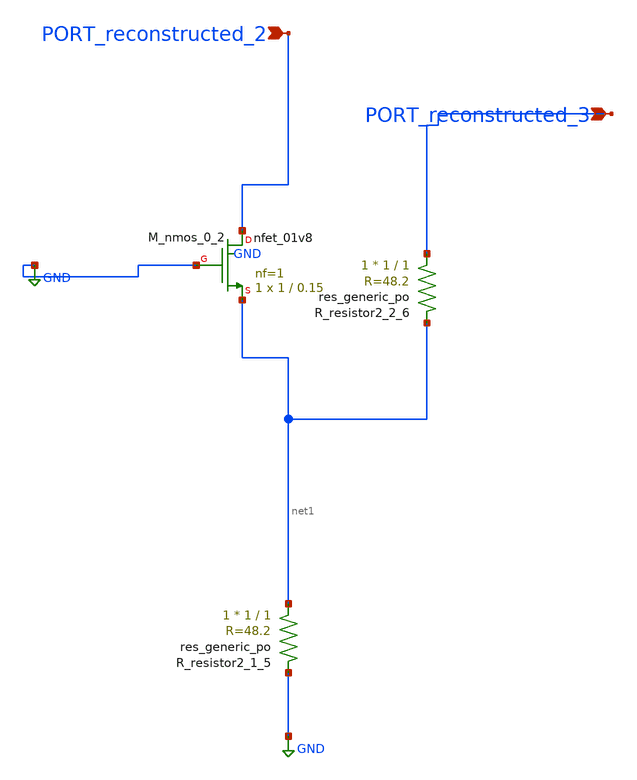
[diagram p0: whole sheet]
** sch_path: schematics/AMSNet/93.sch
**.subckt 93 PORT_reconstructed_2 PORT_reconstructed_3
*.ipin PORT_reconstructed_2
*.ipin PORT_reconstructed_3
XM_nmos_0_2 PORT_reconstructed_2 GND net1 GND sky130_fd_pr__nfet_01v8 L=0.15 W=1 nf=1 ad='int((1 + 1)/2) * 1 / 1 * 0.29'
+ as='int((1 + 2)/2) * 1 / 1 * 0.29' pd='2*int((1 + 1)/2) * (1 / 1 + 0.29)' ps='2*int((1 + 2)/2) * (1 / 1 + 0.29)'
+ nrd='0.29 / 1 ' nrs='0.29 / 1 ' sa=0 sb=0 sd=0 mult=1 m=1
XR_resistor2_1_5 net1 GND sky130_fd_pr__res_generic_po W=1 L=1 m=1
XR_resistor2_2_6 PORT_reconstructed_3 net1 sky130_fd_pr__res_generic_po W=1 L=1 m=1
**.ends
.GLOBAL GND
.end
